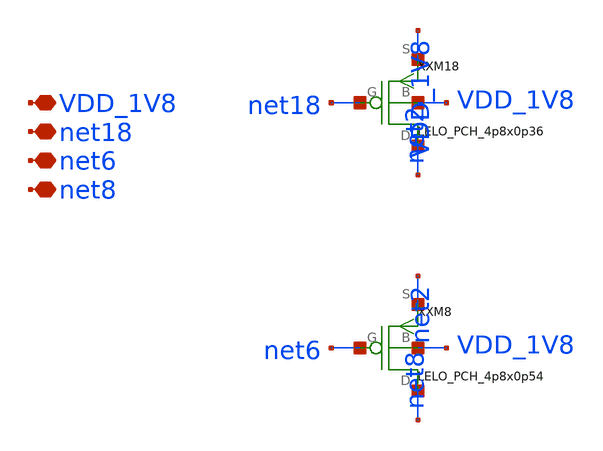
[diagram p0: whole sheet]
** sch_path: design/LELO_VCO_SKY130A/LELO_VCO_PA3.sch
**.subckt LELO_VCO_PA3 VDD_1V8 net18 net6 net8
*.iopin VDD_1V8
*.iopin net18
*.iopin net6
*.iopin net8
XXXM18 net2 net18 VDD_1V8 VDD_1V8 LELO_PCH_4p8x0p36
XXM8 net8 net6 net2 VDD_1V8 LELO_PCH_4p8x0p54
**.ends

* expanding   symbol:  LELO_VCO_SKY130A/LELO_PCH_4p8x0p36.sym # of pins=4
** sym_path: design/LELO_VCO_SKY130A/LELO_PCH_4p8x0p36.sym
** sch_path: design/LELO_VCO_SKY130A/LELO_PCH_4p8x0p36.sch
.subckt LELO_PCH_4p8x0p36 D G S B
*.iopin D
*.iopin G
*.iopin S
*.iopin B
XM1 D G S B sky130_fd_pr__pfet_01v8 L=0.36 W=4.8 nf=1 ad='int((nf+1)/2) * W/nf * 0.29' as='int((nf+2)/2) * W/nf * 0.29'
+ pd='2*int((nf+1)/2) * (W/nf + 0.29)' ps='2*int((nf+2)/2) * (W/nf + 0.29)' nrd='0.29 / W' nrs='0.29 / W'
+ sa=0 sb=0 sd=0 mult=1 m=1
.ends


* expanding   symbol:  LELO_VCO_SKY130A/LELO_PCH_4p8x0p54.sym # of pins=4
** sym_path: design/LELO_VCO_SKY130A/LELO_PCH_4p8x0p54.sym
** sch_path: design/LELO_VCO_SKY130A/LELO_PCH_4p8x0p54.sch
.subckt LELO_PCH_4p8x0p54 D G S B
*.iopin D
*.iopin G
*.iopin S
*.iopin B
XM1 D G S B sky130_fd_pr__pfet_01v8 L=0.54 W=4.8 nf=1 ad='int((nf+1)/2) * W/nf * 0.29' as='int((nf+2)/2) * W/nf * 0.29'
+ pd='2*int((nf+1)/2) * (W/nf + 0.29)' ps='2*int((nf+2)/2) * (W/nf + 0.29)' nrd='0.29 / W' nrs='0.29 / W'
+ sa=0 sb=0 sd=0 mult=1 m=1
.ends

.end
